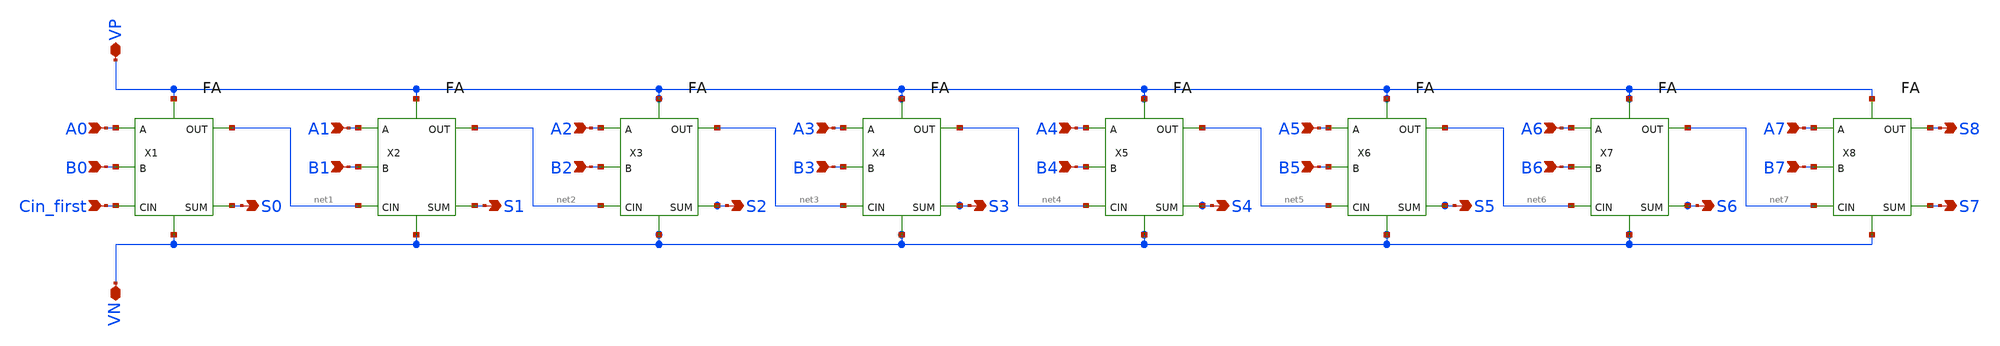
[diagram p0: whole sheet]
** sch_path: projekat_spice/layout/fa_8bits/FA_8bits.sch
* projekat_spice/layout/fa/FA.sym:
* Copyright 2022 Stefan Frederik Schippers
* Licensed under the Apache License, Version 2.0 (the "License");
**.subckt FA_8bits A0 B0 A1 B1 S0 S1 VP VN Cin_first A2 B2 S2 A3 B3 S3 A4 B4 S4 A5 B5 S5 A6 B6 S6 S7
*+ A7 B7 S8
*.ipin A0
*.ipin B0
*.ipin A1
*.ipin B1
*.opin S0
*.opin S1
*.iopin VP
*.iopin VN
*.ipin Cin_first
*.ipin A2
*.ipin B2
*.opin S2
*.ipin A3
*.ipin B3
*.opin S3
*.ipin A4
*.ipin B4
*.opin S4
*.ipin A5
*.ipin B5
*.opin S5
*.ipin A6
*.ipin B6
*.opin S6
*.opin S7
*.ipin A7
*.ipin B7
*.opin S8
X1 A0 B0 Cin_first net1 S0 VP VN FA
X2 A1 B1 net1 net2 S1 VP VN FA
X3 A2 B2 net2 net3 S2 VP VN FA
X4 A3 B3 net3 net4 S3 VP VN FA
X5 A4 B4 net4 net5 S4 VP VN FA
X6 A5 B5 net5 net6 S5 VP VN FA
X7 A6 B6 net6 net7 S6 VP VN FA
X8 A7 B7 net7 S8 S7 VP VN FA
**.ends

* expanding   symbol:  /home/mihailo/projekat_sky130/projekat_layout/fa/FA.sym # of pins=7
** sym_path: projekat_spice/layout/fa/FA.sym
** sch_path: projekat_spice/layout/fa/FA.sch
.subckt FA A B Cin Out Sum VP VN
*.ipin A
*.opin Sum
*.iopin VP
*.iopin VN
*.opin Out
*.ipin B
*.ipin Cin
X4 A B VN VP net1 XOR
X5 Cin net1 VN VP Sum XOR
X1 Cin net1 net3 VP VN AND
X2 A B net2 VP VN AND
X3 net3 net2 Out VP VN OR
.ends


* expanding   symbol:  /home/mihailo/projekat_sky130/projekat_layout/xor/XOR.sym # of pins=5
** sym_path: projekat_spice/layout/xor/XOR.sym
** sch_path: projekat_spice/layout/xor/XOR.sch
.subckt XOR A B VN VP X
*.ipin A
*.ipin B
*.opin X
*.iopin VN
*.iopin VP
X1 B net3 net1 VP VN AND
X2 net4 A net2 VP VN AND
X3 net1 net2 X VP VN OR
X4 A net3 VP VN invertor
X5 B net4 VP VN invertor
.ends


* expanding   symbol:  /home/mihailo/projekat_sky130/projekat_layout/and/AND.sym # of pins=5
** sym_path: projekat_spice/layout/and/AND.sym
** sch_path: projekat_spice/layout/and/AND.sch
.subckt AND A B X VP VN
*.ipin A
*.ipin B
*.iopin VN
*.iopin VP
*.opin X
XM1 net1 A net2 VN sky130_fd_pr__nfet_01v8 L=0.15 W=1 nf=1 ad='int((nf+1)/2) * W/nf * 0.29' as='int((nf+2)/2) * W/nf * 0.29'
+ pd='2*int((nf+1)/2) * (W/nf + 0.29)' ps='2*int((nf+2)/2) * (W/nf + 0.29)' nrd='0.29 / W' nrs='0.29 / W'
+ sa=0 sb=0 sd=0 mult=1 m=1
XM2 net1 A VP VP sky130_fd_pr__pfet_01v8 L=0.15 W=1 nf=1 ad='int((nf+1)/2) * W/nf * 0.29' as='int((nf+2)/2) * W/nf * 0.29'
+ pd='2*int((nf+1)/2) * (W/nf + 0.29)' ps='2*int((nf+2)/2) * (W/nf + 0.29)' nrd='0.29 / W' nrs='0.29 / W'
+ sa=0 sb=0 sd=0 mult=1 m=1
XM3 net1 B VP VP sky130_fd_pr__pfet_01v8 L=0.15 W=1 nf=1 ad='int((nf+1)/2) * W/nf * 0.29' as='int((nf+2)/2) * W/nf * 0.29'
+ pd='2*int((nf+1)/2) * (W/nf + 0.29)' ps='2*int((nf+2)/2) * (W/nf + 0.29)' nrd='0.29 / W' nrs='0.29 / W'
+ sa=0 sb=0 sd=0 mult=1 m=1
XM4 net2 B VN VN sky130_fd_pr__nfet_01v8 L=0.15 W=1 nf=1 ad='int((nf+1)/2) * W/nf * 0.29' as='int((nf+2)/2) * W/nf * 0.29'
+ pd='2*int((nf+1)/2) * (W/nf + 0.29)' ps='2*int((nf+2)/2) * (W/nf + 0.29)' nrd='0.29 / W' nrs='0.29 / W'
+ sa=0 sb=0 sd=0 mult=1 m=1
XM5 X net1 VN VN sky130_fd_pr__nfet_01v8 L=0.15 W=1 nf=1 ad='int((nf+1)/2) * W/nf * 0.29' as='int((nf+2)/2) * W/nf * 0.29'
+ pd='2*int((nf+1)/2) * (W/nf + 0.29)' ps='2*int((nf+2)/2) * (W/nf + 0.29)' nrd='0.29 / W' nrs='0.29 / W'
+ sa=0 sb=0 sd=0 mult=1 m=1
XM6 X net1 VP VP sky130_fd_pr__pfet_01v8 L=0.15 W=1 nf=1 ad='int((nf+1)/2) * W/nf * 0.29' as='int((nf+2)/2) * W/nf * 0.29'
+ pd='2*int((nf+1)/2) * (W/nf + 0.29)' ps='2*int((nf+2)/2) * (W/nf + 0.29)' nrd='0.29 / W' nrs='0.29 / W'
+ sa=0 sb=0 sd=0 mult=1 m=1
.ends


* expanding   symbol:  /home/mihailo/projekat_sky130/projekat_layout/or/OR.sym # of pins=5
** sym_path: projekat_spice/layout/or/OR.sym
** sch_path: projekat_spice/layout/or/OR.sch
.subckt OR A B X VP VN
*.opin X
*.ipin A
*.ipin B
*.iopin VP
*.iopin VN
XM1 net2 A VN VN sky130_fd_pr__nfet_01v8 L=0.15 W=1 nf=1 ad='int((nf+1)/2) * W/nf * 0.29' as='int((nf+2)/2) * W/nf * 0.29'
+ pd='2*int((nf+1)/2) * (W/nf + 0.29)' ps='2*int((nf+2)/2) * (W/nf + 0.29)' nrd='0.29 / W' nrs='0.29 / W'
+ sa=0 sb=0 sd=0 mult=1 m=1
XM2 net1 A VP VP sky130_fd_pr__pfet_01v8 L=0.15 W=1 nf=1 ad='int((nf+1)/2) * W/nf * 0.29' as='int((nf+2)/2) * W/nf * 0.29'
+ pd='2*int((nf+1)/2) * (W/nf + 0.29)' ps='2*int((nf+2)/2) * (W/nf + 0.29)' nrd='0.29 / W' nrs='0.29 / W'
+ sa=0 sb=0 sd=0 mult=1 m=1
XM3 net2 B net1 VP sky130_fd_pr__pfet_01v8 L=0.15 W=1 nf=1 ad='int((nf+1)/2) * W/nf * 0.29' as='int((nf+2)/2) * W/nf * 0.29'
+ pd='2*int((nf+1)/2) * (W/nf + 0.29)' ps='2*int((nf+2)/2) * (W/nf + 0.29)' nrd='0.29 / W' nrs='0.29 / W'
+ sa=0 sb=0 sd=0 mult=1 m=1
XM4 net2 B VN VN sky130_fd_pr__nfet_01v8 L=0.15 W=1 nf=1 ad='int((nf+1)/2) * W/nf * 0.29' as='int((nf+2)/2) * W/nf * 0.29'
+ pd='2*int((nf+1)/2) * (W/nf + 0.29)' ps='2*int((nf+2)/2) * (W/nf + 0.29)' nrd='0.29 / W' nrs='0.29 / W'
+ sa=0 sb=0 sd=0 mult=1 m=1
XM5 X net2 VN VN sky130_fd_pr__nfet_01v8 L=0.15 W=1 nf=1 ad='int((nf+1)/2) * W/nf * 0.29' as='int((nf+2)/2) * W/nf * 0.29'
+ pd='2*int((nf+1)/2) * (W/nf + 0.29)' ps='2*int((nf+2)/2) * (W/nf + 0.29)' nrd='0.29 / W' nrs='0.29 / W'
+ sa=0 sb=0 sd=0 mult=1 m=1
XM6 X net2 VP VP sky130_fd_pr__pfet_01v8 L=0.15 W=1 nf=1 ad='int((nf+1)/2) * W/nf * 0.29' as='int((nf+2)/2) * W/nf * 0.29'
+ pd='2*int((nf+1)/2) * (W/nf + 0.29)' ps='2*int((nf+2)/2) * (W/nf + 0.29)' nrd='0.29 / W' nrs='0.29 / W'
+ sa=0 sb=0 sd=0 mult=1 m=1
.ends


* expanding   symbol:  /home/mihailo/projekat_sky130/projekat_layout/invertor/invertor.sym # of
*+ pins=4
** sym_path: projekat_spice/layout/invertor/invertor.sym
** sch_path: projekat_spice/layout/invertor/invertor.sch
.subckt invertor A Y VP VN
*.iopin VP
*.iopin VN
*.ipin A
*.opin Y
XM1 Y A VN VN sky130_fd_pr__nfet_01v8 L=0.15 W=1 nf=1 ad='int((nf+1)/2) * W/nf * 0.29' as='int((nf+2)/2) * W/nf * 0.29'
+ pd='2*int((nf+1)/2) * (W/nf + 0.29)' ps='2*int((nf+2)/2) * (W/nf + 0.29)' nrd='0.29 / W' nrs='0.29 / W'
+ sa=0 sb=0 sd=0 mult=1 m=1
XM2 Y A VP VP sky130_fd_pr__pfet_01v8 L=0.15 W=1 nf=1 ad='int((nf+1)/2) * W/nf * 0.29' as='int((nf+2)/2) * W/nf * 0.29'
+ pd='2*int((nf+1)/2) * (W/nf + 0.29)' ps='2*int((nf+2)/2) * (W/nf + 0.29)' nrd='0.29 / W' nrs='0.29 / W'
+ sa=0 sb=0 sd=0 mult=1 m=1
.ends

.end
